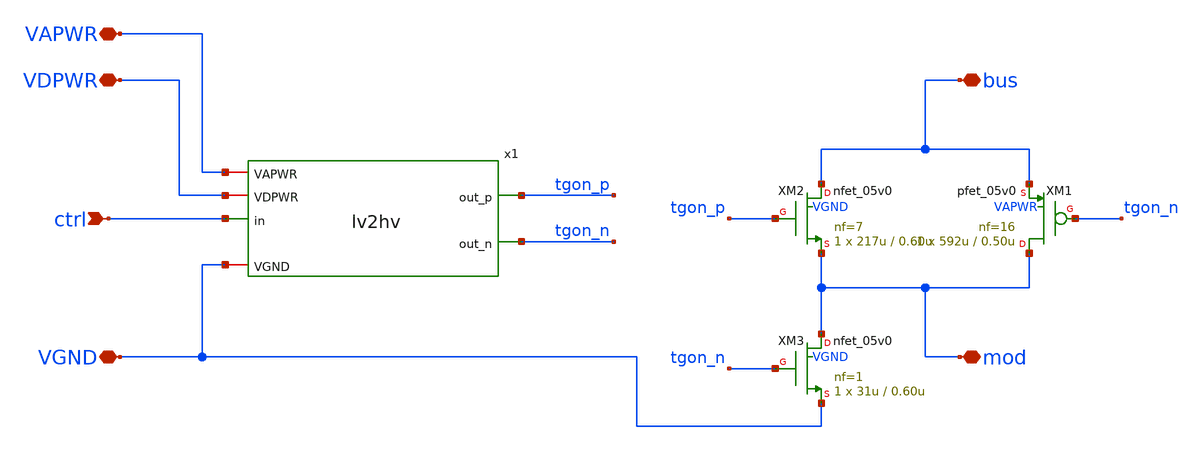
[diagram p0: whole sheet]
** sch_path: asw/gf180mcuD/tt_asw_5v0/xschem/tt_asw_5v0.sch
**.subckt tt_asw_5v0 ctrl VDPWR VGND mod VAPWR bus
*.ipin ctrl
*.iopin VDPWR
*.iopin VGND
*.iopin mod
*.iopin VAPWR
*.iopin bus
x1 VGND VDPWR VAPWR ctrl tgon_p tgon_n lv2hv
XM1 mod tgon_n bus VAPWR pfet_05v0 L=0.50u W=592u nf=16 ad='int((nf+1)/2) * W/nf * 0.18u' as='int((nf+2)/2) * W/nf * 0.18u'
+ pd='2*int((nf+1)/2) * (W/nf + 0.18u)' ps='2*int((nf+2)/2) * (W/nf + 0.18u)' nrd='0.18u / W' nrs='0.18u / W'
+ sa=0 sb=0 sd=0 m=1 par=1
XM2 bus tgon_p mod VGND nfet_05v0 L=0.60u W=217u nf=7 ad='int((nf+1)/2) * W/nf * 0.18u' as='int((nf+2)/2) * W/nf * 0.18u'
+ pd='2*int((nf+1)/2) * (W/nf + 0.18u)' ps='2*int((nf+2)/2) * (W/nf + 0.18u)' nrd='0.18u / W' nrs='0.18u / W'
+ sa=0 sb=0 sd=0 m=1 par=1
XM3 mod tgon_n VGND VGND nfet_05v0 L=0.60u W=31u nf=1 ad='int((nf+1)/2) * W/nf * 0.18u' as='int((nf+2)/2) * W/nf * 0.18u'
+ pd='2*int((nf+1)/2) * (W/nf + 0.18u)' ps='2*int((nf+2)/2) * (W/nf + 0.18u)' nrd='0.18u / W' nrs='0.18u / W'
+ sa=0 sb=0 sd=0 m=1 par=1
**.ends
.end
